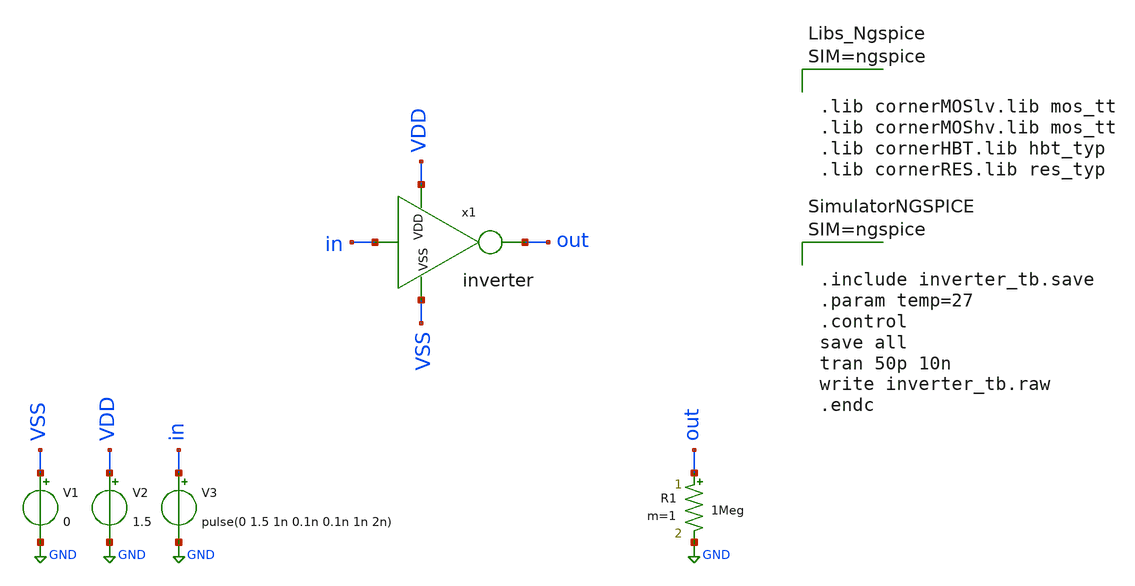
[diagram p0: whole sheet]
** sch_path: inverter/inverter_tb.sch
**.subckt inverter_tb
x1 in out VDD VSS inverter
R1 out GND 1Meg m=1
V1 VSS GND 0
V2 VDD GND 1.5
V3 in GND pulse(0 1.5 1n 0.1n 0.1n 1n 2n)
**** begin user architecture code



.lib cornerMOSlv.lib mos_tt
.lib cornerMOShv.lib mos_tt
.lib cornerHBT.lib hbt_typ
.lib cornerRES.lib res_typ






.include inverter_tb.save
.param temp=27
.control
save all
tran 50p 10n
write inverter_tb.raw
.endc



**** end user architecture code
**.ends

* expanding   symbol:  inverter.sym # of pins=4
** sym_path: inverter/inverter.sym
** sch_path: inverter/inverter.sch
.subckt inverter in out VDD VSS
*.ipin in
*.ipin VDD
*.ipin VSS
*.opin out
XM1 out in VSS VSS sg13_lv_nmos w=0.15u l=0.13u ng=1 m=1 mm_ok=1
XM2 out in VDD VDD sg13_lv_pmos w=0.15u l=0.13u ng=1 m=1 mm_ok=1
.ends

.GLOBAL GND
.end
